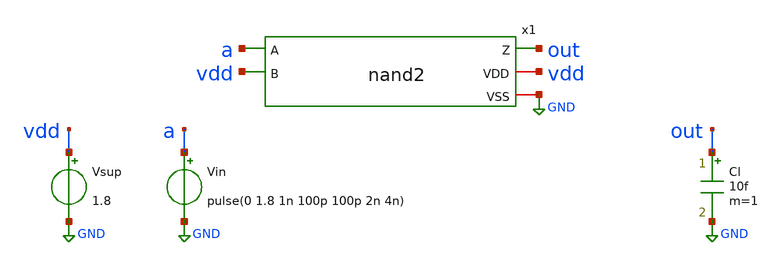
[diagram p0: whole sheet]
** sch_path: pipeline/analog/nand2/nand2_tb.sch
**.subckt nand2_tb
x1 a vdd out vdd GND nand2
Vsup vdd GND 1.8
Vin a GND pulse(0 1.8 1n 100p 100p 2n 4n)
Cl out GND 10f m=1
**** begin user architecture code


%PDK_LIB%



.param W_P=1.0 W_N=0.5 L_P=0.15 L_N=0.15
.control
dc Vin 0 1.8 0.01
meas dc vtrip WHEN v(out)=0.9 FALL=1
tran 10p 8n
meas tran tphl TRIG v(a) VAL=0.9 RISE=1 TARG v(out) VAL=0.9 FALL=1
meas tran tplh TRIG v(a) VAL=0.9 FALL=1 TARG v(out) VAL=0.9 RISE=1
meas tran ivdd_avg AVG i(Vsup) FROM=0 TO=8n
quit
.endc


**** end user architecture code
**.ends

* expanding   symbol:  nand2/nand2.sym # of pins=5
** sym_path: pipeline/analog/nand2/nand2.sym
** sch_path: pipeline/analog/nand2/nand2.sch
.subckt nand2 A B Z VDD VSS
*.ipin A
*.ipin B
*.opin Z
*.iopin VDD
*.iopin VSS
XM1 Z A ni VSS sky130_fd_pr__nfet_01v8 L=L_N W=W_N nf=1 ad='int((nf+1)/2) * W/nf * 0.29' as='int((nf+2)/2) * W/nf * 0.29'
+ pd='2*int((nf+1)/2) * (W/nf + 0.29)' ps='2*int((nf+2)/2) * (W/nf + 0.29)' nrd='0.29 / W' nrs='0.29 / W'
+ sa=0 sb=0 sd=0 mult=1 m=1
XM2 ni B VSS VSS sky130_fd_pr__nfet_01v8 L=L_N W=W_N nf=1 ad='int((nf+1)/2) * W/nf * 0.29' as='int((nf+2)/2) * W/nf * 0.29'
+ pd='2*int((nf+1)/2) * (W/nf + 0.29)' ps='2*int((nf+2)/2) * (W/nf + 0.29)' nrd='0.29 / W' nrs='0.29 / W'
+ sa=0 sb=0 sd=0 mult=1 m=1
XM3 Z A VDD VDD sky130_fd_pr__pfet_01v8 L=L_P W=W_P nf=1 ad='int((nf+1)/2) * W/nf * 0.29' as='int((nf+2)/2) * W/nf * 0.29'
+ pd='2*int((nf+1)/2) * (W/nf + 0.29)' ps='2*int((nf+2)/2) * (W/nf + 0.29)' nrd='0.29 / W' nrs='0.29 / W'
+ sa=0 sb=0 sd=0 mult=1 m=1
XM4 Z B VDD VDD sky130_fd_pr__pfet_01v8 L=L_P W=W_P nf=1 ad='int((nf+1)/2) * W/nf * 0.29' as='int((nf+2)/2) * W/nf * 0.29'
+ pd='2*int((nf+1)/2) * (W/nf + 0.29)' ps='2*int((nf+2)/2) * (W/nf + 0.29)' nrd='0.29 / W' nrs='0.29 / W'
+ sa=0 sb=0 sd=0 mult=1 m=1
.ends

.GLOBAL GND
.end
